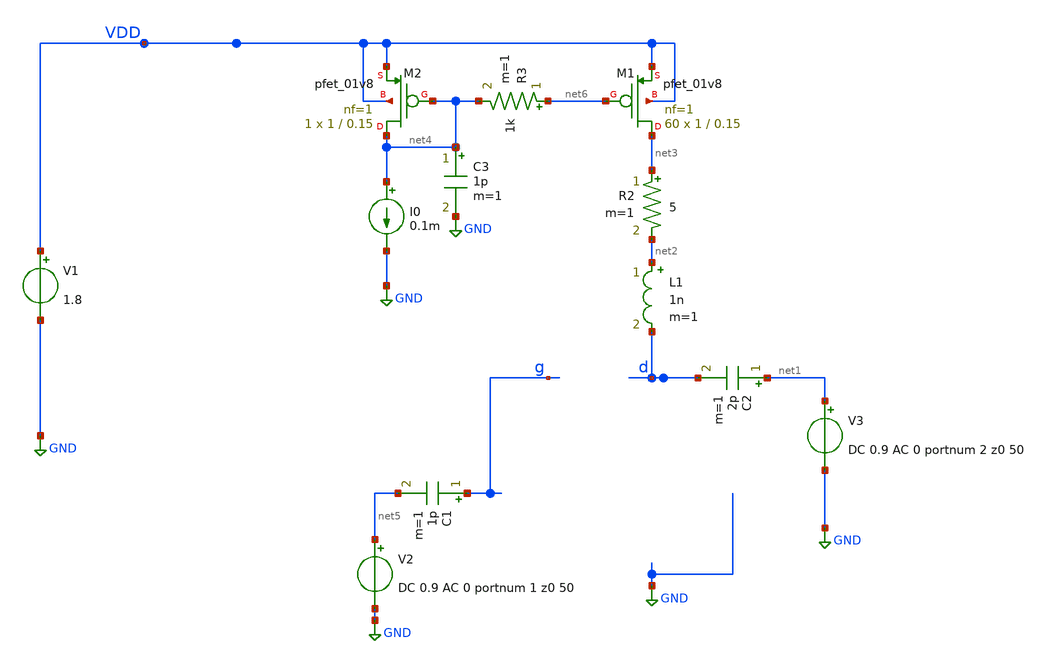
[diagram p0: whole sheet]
** sch_path: xschem/dumb_amp_r1_2_PEX.sch
**.subckt dumb_amp_r1_2_PEX
V1 VDD GND 1.8
V3 net1 GND DC 0.9 AC 0 portnum 2 z0 50
V2 net5 GND DC 0.9 AC 0 portnum 1 z0 50
C1 g net5 1p m=1
C2 net1 d 2p m=1
L1 net2 d 1n m=1
R2 net3 net2 5 m=1
XM1 net3 net6 VDD VDD sky130_fd_pr__pfet_01v8 L=0.15 W=1 nf=1 ad='int((nf+1)/2) * W/nf * 0.29' as='int((nf+2)/2) * W/nf * 0.29'
+ pd='2*int((nf+1)/2) * (W/nf + 0.29)' ps='2*int((nf+2)/2) * (W/nf + 0.29)' nrd='0.29 / W' nrs='0.29 / W'
+ sa=0 sb=0 sd=0 mult=60 m=60
XM2 net4 net4 VDD VDD sky130_fd_pr__pfet_01v8 L=0.15 W=1 nf=1 ad='int((nf+1)/2) * W/nf * 0.29' as='int((nf+2)/2) * W/nf * 0.29'
+ pd='2*int((nf+1)/2) * (W/nf + 0.29)' ps='2*int((nf+2)/2) * (W/nf + 0.29)' nrd='0.29 / W' nrs='0.29 / W'
+ sa=0 sb=0 sd=0 mult=1 m=1
I0 net4 GND 0.1m
C3 net4 GND 1p m=1
R3 net6 net4 1k m=1
**** begin user architecture code
.lib $::SKYWATER_MODELS/sky130.lib.spice tt
* .include $::PDKPATH/libs.ref/sky130_fd_sc_hvl/spice/sky130_fd_sc_hvl.spice


.subckt DUT NGATE NDRAIN VSUBS
.subckt sky130_fd_pr__rf_nfet_01v8_aM02W5p00L0p15 DRAIN GATE SOURCE SUBSTRATE
X0 DRAIN GATE SOURCE SUBSTRATE sky130_fd_pr__nfet_01v8 ad=1.414e+12p pd=1.066e+07u as=2.828e+12p
+ ps=2.132e+07u w=5.05e+06u l=150000u
X1 SOURCE GATE DRAIN SUBSTRATE sky130_fd_pr__nfet_01v8 ad=0p pd=0u as=0p ps=0u w=5.05e+06u l=150000u
C0 DRAIN SOURCE 3.59fF
C1 GATE SOURCE 0.46fF
C2 DRAIN GATE 0.34fF
C3 DRAIN SUBSTRATE 0.40fF
C4 SOURCE SUBSTRATE 2.44fF
C5 GATE SUBSTRATE 0.64fF
.ends

.subckt nfet_3x_2 D G S sub
Xsky130_fd_pr__rf_nfet_01v8_aM02W5p00L0p15_0 D G S sub sky130_fd_pr__rf_nfet_01v8_aM02W5p00L0p15
Xsky130_fd_pr__rf_nfet_01v8_aM02W5p00L0p15_1 D G S sub sky130_fd_pr__rf_nfet_01v8_aM02W5p00L0p15
Xsky130_fd_pr__rf_nfet_01v8_aM02W5p00L0p15_2 D G S sub sky130_fd_pr__rf_nfet_01v8_aM02W5p00L0p15
C0 G sub 1.34fF
C1 S D -0.11fF
C2 S G 2.13fF
C3 G D 1.69fF
C4 S sub -0.01fF
C5 D sub -0.05fF
C6 sub 0 -1.34fF
C7 D 0 0.62fF
C8 S 0 6.66fF
C9 G 0 1.96fF
.ends

.subckt RF_nfet_6xaM02W5p0L0p15 G S D B
Xnfet_3x_2_0 D G S B nfet_3x_2
Xnfet_3x_2_1 D G S B nfet_3x_2
C0 D B -0.02fF
C1 G S 0.20fF
C2 G B 0.06fF
C3 G D 0.14fF
C4 S B 0.02fF
C5 D S 0.01fF
C6 B 0 -3.73fF
C7 D 0 1.02fF
C8 S 0 13.03fF
C9 G 0 3.30fF
.ends


.subckt sky130_fd_pr__res_generic_po_JFYRVD a_75_284# a_n141_n357# a_n271_n487#
R0 a_n141_n357# a_75_284# sky130_fd_pr__res_generic_po w=330000u l=6.2e+06u
C0 a_n141_n357# a_n271_n487# 0.14fF
C1 a_75_284# a_n271_n487# 0.14fF
.ends

XRF_nfet_6xaM02W5p0L0p15_0 NGATE NDRAIN VSUBS VSUBS RF_nfet_6xaM02W5p0L0p15
Xsky130_fd_pr__res_generic_po_JFYRVD_0 NGATE NDRAIN VSUBS sky130_fd_pr__res_generic_po_JFYRVD
C0 VSUBS NDRAIN 1.42fF
C1 NGATE VSUBS 2.81fF
C2 NGATE NDRAIN 2.91fF
C5 NDRAIN VSUBS 14.22fF
C6 NGATE VSUBS 3.28fF
.ends

XDUT G D GND DUT




.sp dec 1000 1e9 10e9 1


* .ac dec 1000 0.01e9 100e9
.control
run
display

let z11=50*(1+s_1_1)/(1-s_1_1)
let z22=50*(1+s_2_2)/(1-s_2_2)
let S11 = S_1_1
let S21 = S_2_1
let S12 = S_1_2
let S22 = S_2_2

* Stability
let delta=S11*S22-S12*S21
let K    = (1-mag(S11)^2-mag(S22)^2+mag(delta)^2)/(2*mag(S12*S21))
let mu   = (1-mag(S11)^2)/(mag(S22-conj(S11)*delta)+mag(S21*S12))
* plot real(z11) real(z22)
* plot imag(z11) imag(z22)
plot db(S_1_1) db(S_2_2) db(S_2_1)
*
plot db(K)
plot mag(delta)
plot db(mu)
plot NF NFmin
.endc


**** end user architecture code
**.ends
.GLOBAL GND
.end
